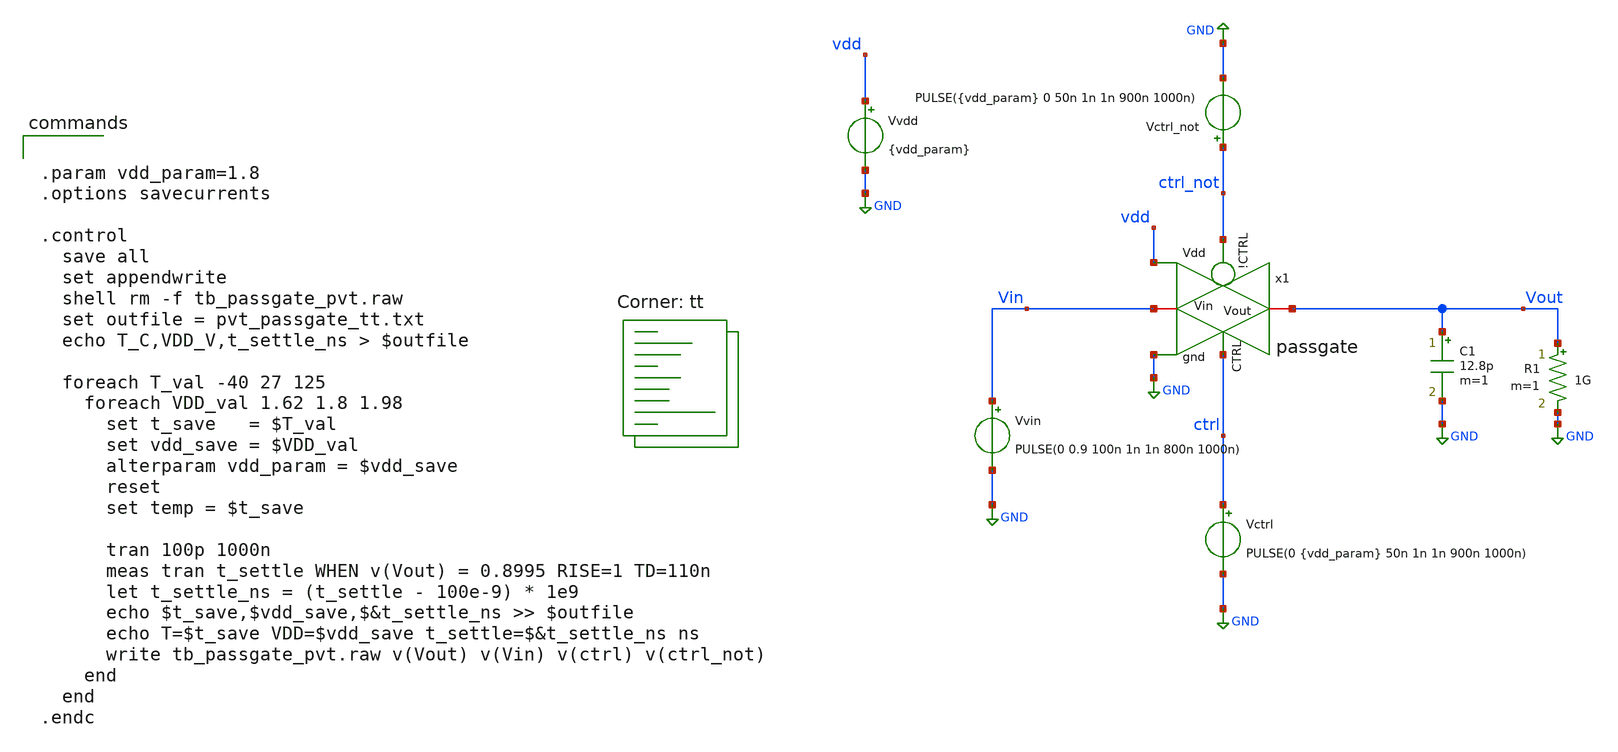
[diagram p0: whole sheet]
** sch_path: 05_mixed_signal/soluzioni/lab01/xschem/tb_passgate_pvt.sch
**.subckt tb_passgate_pvt
Vvdd vdd GND {vdd_param}
x1 Vin GND ctrl_not ctrl vdd Vout passgate
Vvin Vin GND PULSE(0 0.9 100n 1n 1n 800n 1000n)
Vctrl ctrl GND PULSE(0 {vdd_param} 50n 1n 1n 900n 1000n)
Vctrl_not ctrl_not GND PULSE({vdd_param} 0 50n 1n 1n 900n 1000n)
C1 Vout GND 12.8p m=1
R1 Vout GND 1G m=1
**** begin user architecture code


.param vdd_param=1.8
.options savecurrents

.control
  save all
  set appendwrite
  shell rm -f tb_passgate_pvt.raw
  set outfile = pvt_passgate_tt.txt
  echo T_C,VDD_V,t_settle_ns > $outfile

  foreach T_val -40 27 125
    foreach VDD_val 1.62 1.8 1.98
      set t_save   = $T_val
      set vdd_save = $VDD_val
      alterparam vdd_param = $vdd_save
      reset
      set temp = $t_save

      tran 100p 1000n
      meas tran t_settle WHEN v(Vout) = 0.8995 RISE=1 TD=110n
      let t_settle_ns = (t_settle - 100e-9) * 1e9
      echo $t_save,$vdd_save,$&t_settle_ns >> $outfile
      echo T=$t_save VDD=$vdd_save t_settle=$&t_settle_ns ns
      write tb_passgate_pvt.raw v(Vout) v(Vin) v(ctrl) v(ctrl_not)
    end
  end
.endc


.lib $::SKYWATER_MODELS/sky130.lib.spice tt
**** end user architecture code
**.ends

* expanding   symbol:  passgate.sym # of pins=6
** sym_path: 05_mixed_signal/soluzioni/lab03/xschem/passgate.sym
** sch_path: 05_mixed_signal/soluzioni/lab03/xschem/passgate.sch
.subckt passgate Vin gnd !CTRL CTRL Vdd Vout
*.ipin CTRL
*.ipin !CTRL
*.iopin Vin
*.iopin Vout
*.ipin Vdd
*.ipin gnd
XM3 Vin CTRL Vout gnd sky130_fd_pr__nfet_01v8_lvt L=0.15 W=6 nf=1 ad='int((1 + 1)/2) * 6 / 1 * 0.29'
+ as='int((1 + 2)/2) * 6 / 1 * 0.29' pd='2*int((1 + 1)/2) * (6 / 1 + 0.29)' ps='2*int((1 + 2)/2) * (6 / 1 + 0.29)'
+ nrd='0.29 / 6 ' nrs='0.29 / 6 ' sa=0 sb=0 sd=0 mult=1 m=1
XM1 Vin !CTRL Vout Vdd sky130_fd_pr__pfet_01v8_lvt L=0.35 W=12 nf=1 ad='int((1 + 1)/2) * 12 / 1 * 0.29'
+ as='int((1 + 2)/2) * 12 / 1 * 0.29' pd='2*int((1 + 1)/2) * (12 / 1 + 0.29)' ps='2*int((1 + 2)/2) * (12 / 1 + 0.29)'
+ nrd='0.29 / 12 ' nrs='0.29 / 12 ' sa=0 sb=0 sd=0 mult=1 m=1
.ends

.GLOBAL GND
.end
